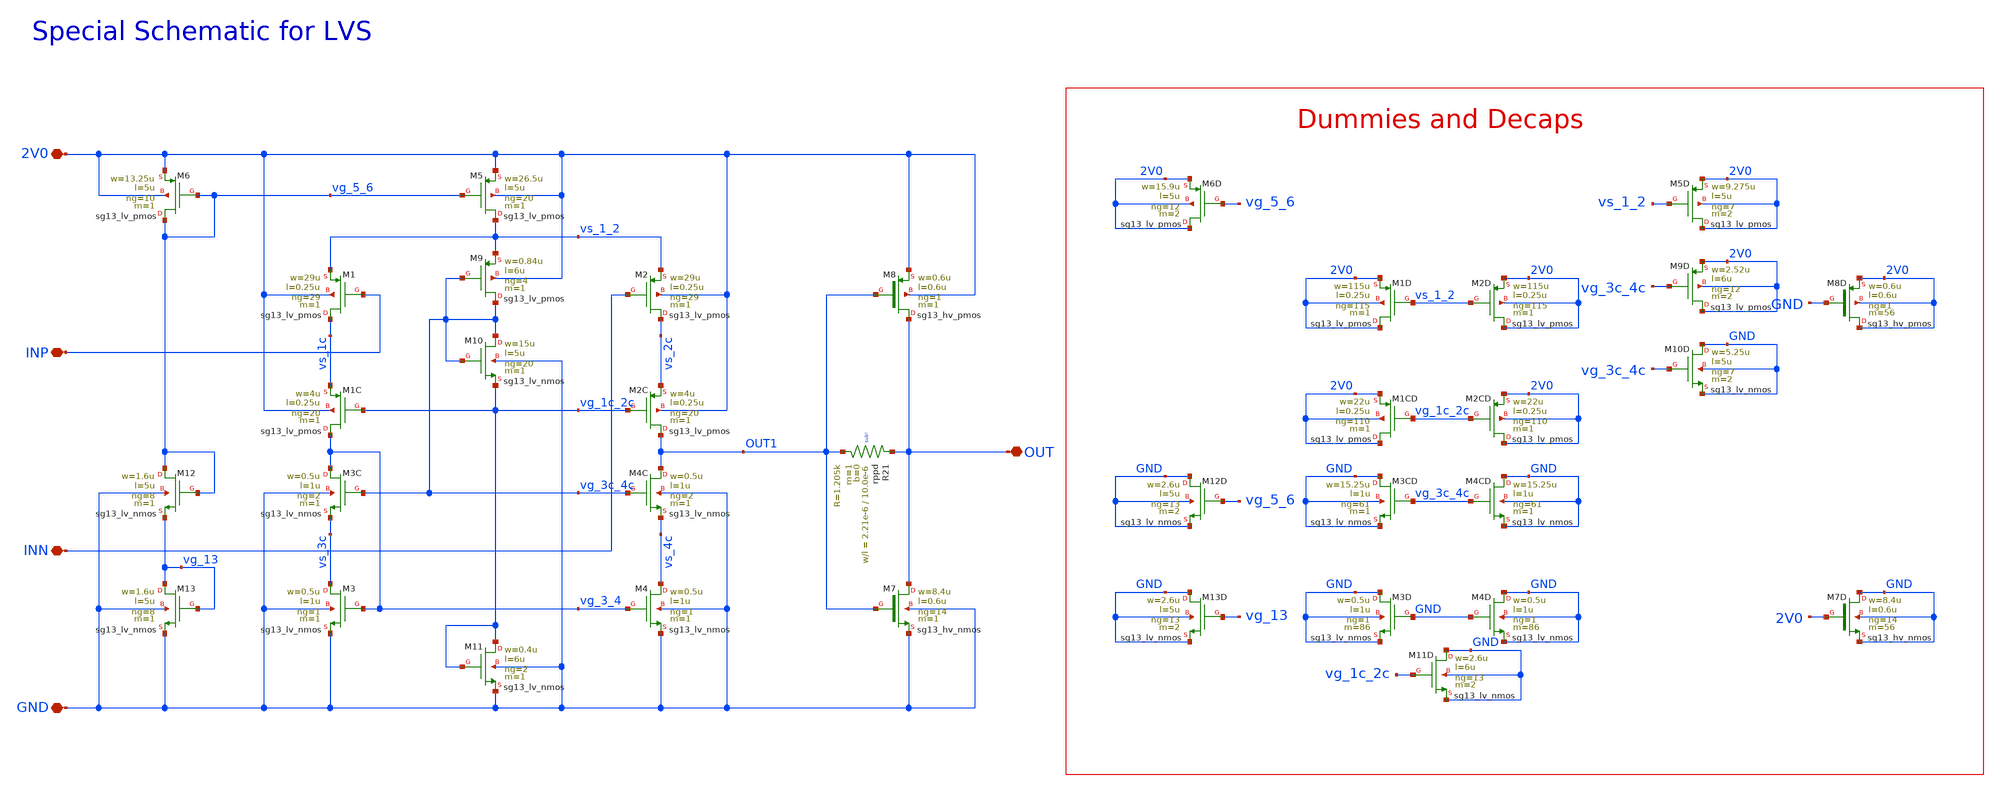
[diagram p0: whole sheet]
** sch_path: mWATTBAT/design_data/lvs/IFAMP_LVS.sch
**.subckt IFAMP_LVS INP INN OUT 2V0 GND
*.iopin INP
*.iopin INN
*.iopin OUT
*.iopin 2V0
*.iopin GND
XM1 vs_1c INP vs_1_2 2V0 sg13_lv_pmos w=29u l=0.25u ng=29 m=1 mm_ok=1
XM2 vs_2c INN vs_1_2 2V0 sg13_lv_pmos w=29u l=0.25u ng=29 m=1 mm_ok=1
XM1C vg_3_4 vg_1c_2c vs_1c 2V0 sg13_lv_pmos w=4u l=0.25u ng=20 m=1 mm_ok=1
XM2C OUT1 vg_1c_2c vs_2c 2V0 sg13_lv_pmos w=4u l=0.25u ng=20 m=1 mm_ok=1
XM3C vg_3_4 vg_3c_4c vs_3c GND sg13_lv_nmos w=0.5u l=1u ng=2 m=1 mm_ok=1
XM4C OUT1 vg_3c_4c vs_4c GND sg13_lv_nmos w=0.5u l=1u ng=2 m=1 mm_ok=1
XM3 vs_3c vg_3_4 GND GND sg13_lv_nmos w=0.5u l=1u ng=1 m=1 mm_ok=1
XM4 vs_4c vg_3_4 GND GND sg13_lv_nmos w=0.5u l=1u ng=1 m=1 mm_ok=1
XM5 vs_1_2 vg_5_6 2V0 2V0 sg13_lv_pmos w=26.5u l=5u ng=20 m=1 mm_ok=1
XM6 vg_5_6 vg_5_6 2V0 2V0 sg13_lv_pmos w=13.25u l=5u ng=10 m=1 mm_ok=1
XM7 OUT OUT1 GND GND sg13_hv_nmos w=8.4u l=0.6u ng=14 m=1 mm_ok=1
XM8 OUT OUT1 2V0 2V0 sg13_hv_pmos w=0.6u l=0.6u ng=1 m=1 mm_ok=1
XM9 vg_3c_4c vg_3c_4c vs_1_2 2V0 sg13_lv_pmos w=0.84u l=6u ng=4 m=1 mm_ok=1
XM10 vg_3c_4c vg_3c_4c vg_1c_2c GND sg13_lv_nmos w=15u l=5u ng=20 m=1 mm_ok=1
XM11 vg_1c_2c vg_1c_2c GND GND sg13_lv_nmos w=0.4u l=6u ng=2 m=1 mm_ok=1
XM13 vg_13 vg_13 GND GND sg13_lv_nmos w=1.6u l=5u ng=8 m=1 mm_ok=1
XM12 vg_5_6 vg_5_6 vg_13 GND sg13_lv_nmos w=1.6u l=5u ng=8 m=1 mm_ok=1
XM13D GND vg_13 GND GND sg13_lv_nmos w=2.6u l=5u ng=13 m=2 mm_ok=1
XM12D GND vg_5_6 GND GND sg13_lv_nmos w=2.6u l=5u ng=13 m=2 mm_ok=1
XM6D 2V0 vg_5_6 2V0 2V0 sg13_lv_pmos w=15.9u l=5u ng=12 m=2 mm_ok=1
XM5D 2V0 vs_1_2 2V0 2V0 sg13_lv_pmos w=9.275u l=5u ng=7 m=2 mm_ok=1
XM11D GND vg_1c_2c GND GND sg13_lv_nmos w=2.6u l=6u ng=13 m=2 mm_ok=1
XM9D 2V0 vg_3c_4c 2V0 2V0 sg13_lv_pmos w=2.52u l=6u ng=12 m=2 mm_ok=1
XM10D GND vg_3c_4c GND GND sg13_lv_nmos w=5.25u l=5u ng=7 m=2 mm_ok=1
XM3CD GND vg_3c_4c GND GND sg13_lv_nmos w=15.25u l=1u ng=61 m=1 mm_ok=1
XM3D GND GND GND GND sg13_lv_nmos w=0.5u l=1u ng=1 m=86 mm_ok=1
XM4CD GND vg_3c_4c GND GND sg13_lv_nmos w=15.25u l=1u ng=61 m=1 mm_ok=1
XM1CD 2V0 vg_1c_2c 2V0 2V0 sg13_lv_pmos w=22u l=0.25u ng=110 m=1 mm_ok=1
XM2CD 2V0 vg_1c_2c 2V0 2V0 sg13_lv_pmos w=22u l=0.25u ng=110 m=1 mm_ok=1
XM1D 2V0 vs_1_2 2V0 2V0 sg13_lv_pmos w=115u l=0.25u ng=115 m=1 mm_ok=1
XM2D 2V0 vs_1_2 2V0 2V0 sg13_lv_pmos w=115u l=0.25u ng=115 m=1 mm_ok=1
XM4D GND GND GND GND sg13_lv_nmos w=0.5u l=1u ng=1 m=86 mm_ok=1
XM7D GND 2V0 GND GND sg13_hv_nmos w=8.4u l=0.6u ng=14 m=56 mm_ok=1
XM8D 2V0 GND 2V0 2V0 sg13_hv_pmos w=0.6u l=0.6u ng=1 m=56 mm_ok=1
XR21 OUT OUT1 sub! rppd w=2.21e-6 l=10.0e-6 m=1 b=0 mm_ok=1
**.ends
.end
